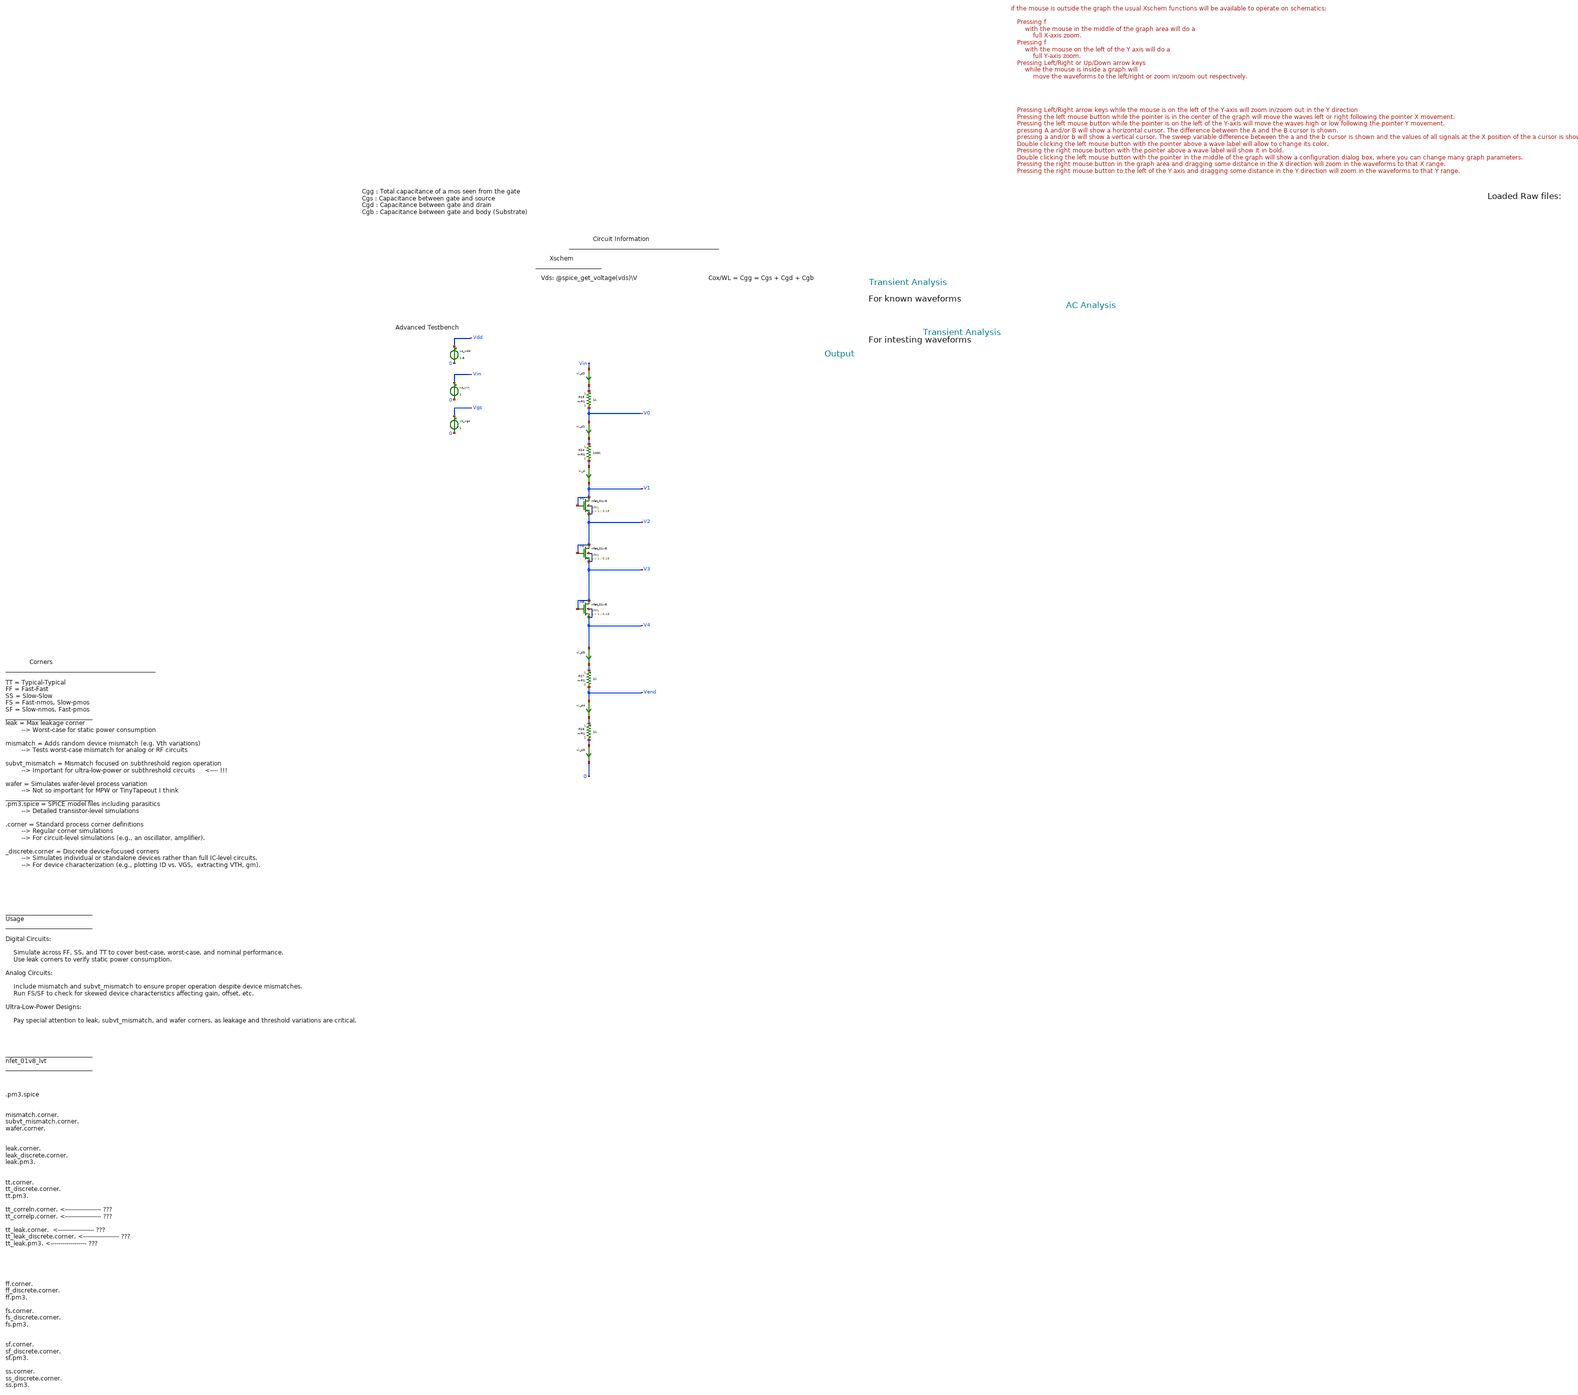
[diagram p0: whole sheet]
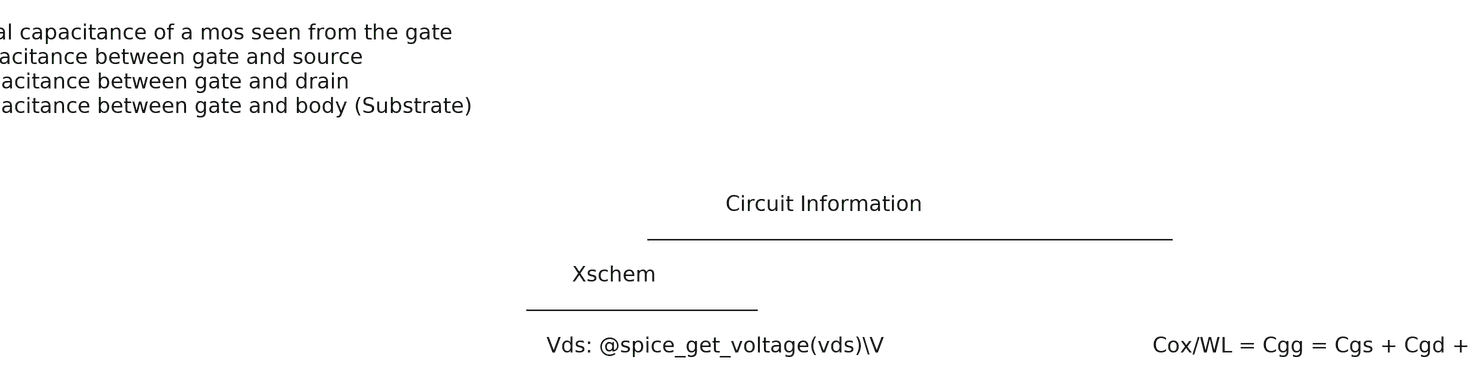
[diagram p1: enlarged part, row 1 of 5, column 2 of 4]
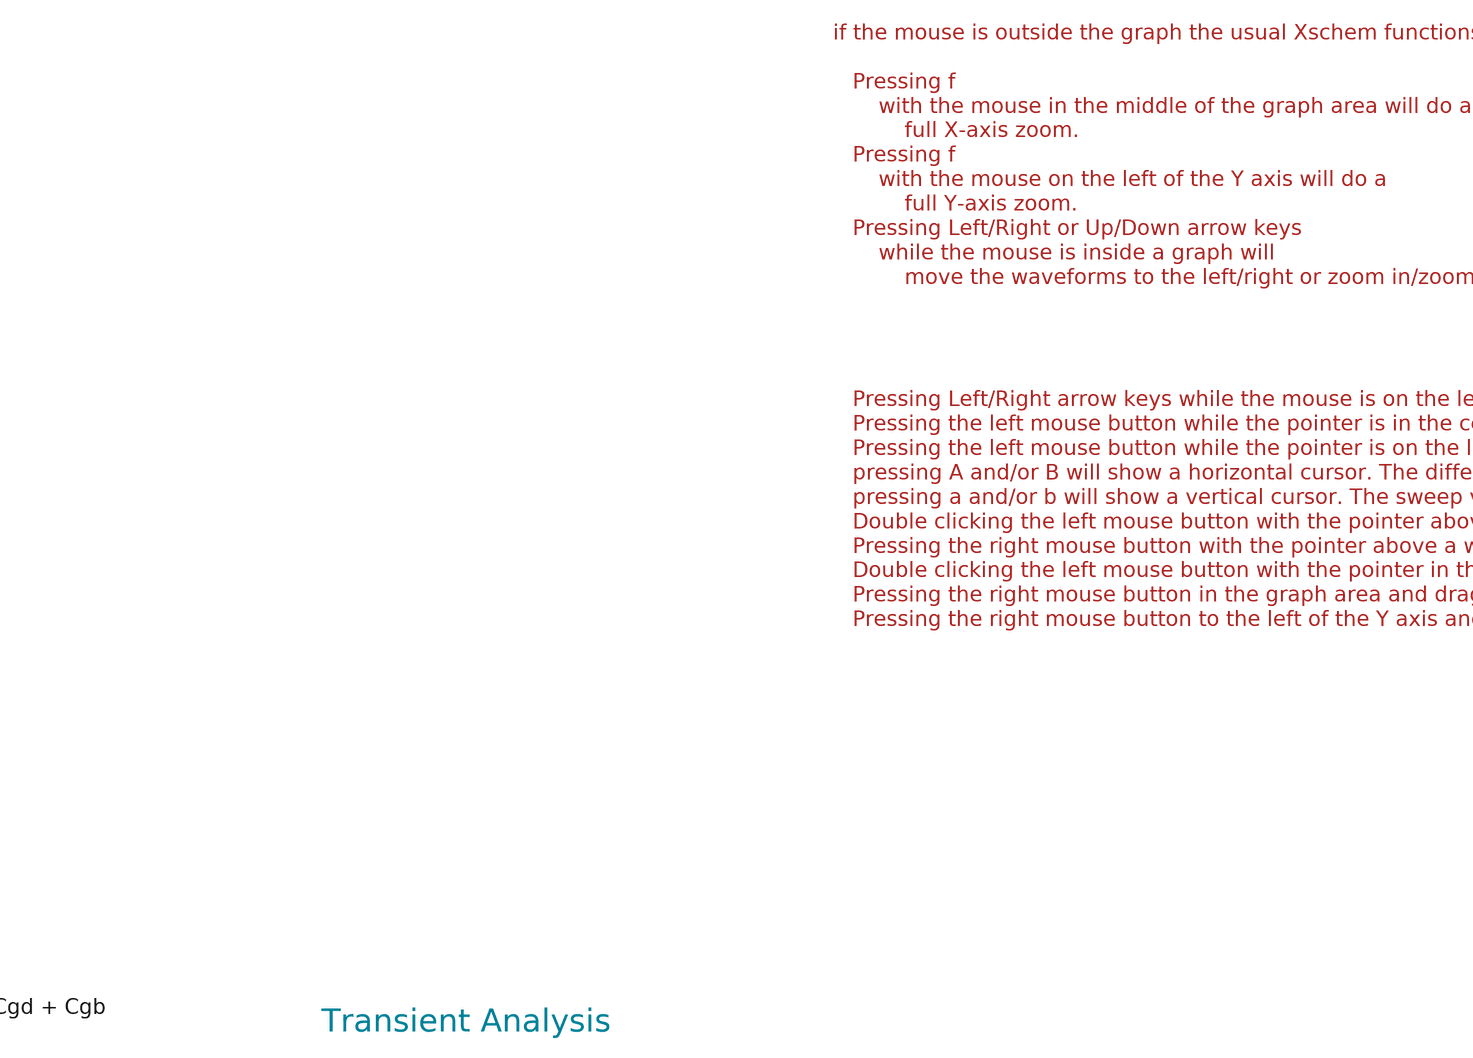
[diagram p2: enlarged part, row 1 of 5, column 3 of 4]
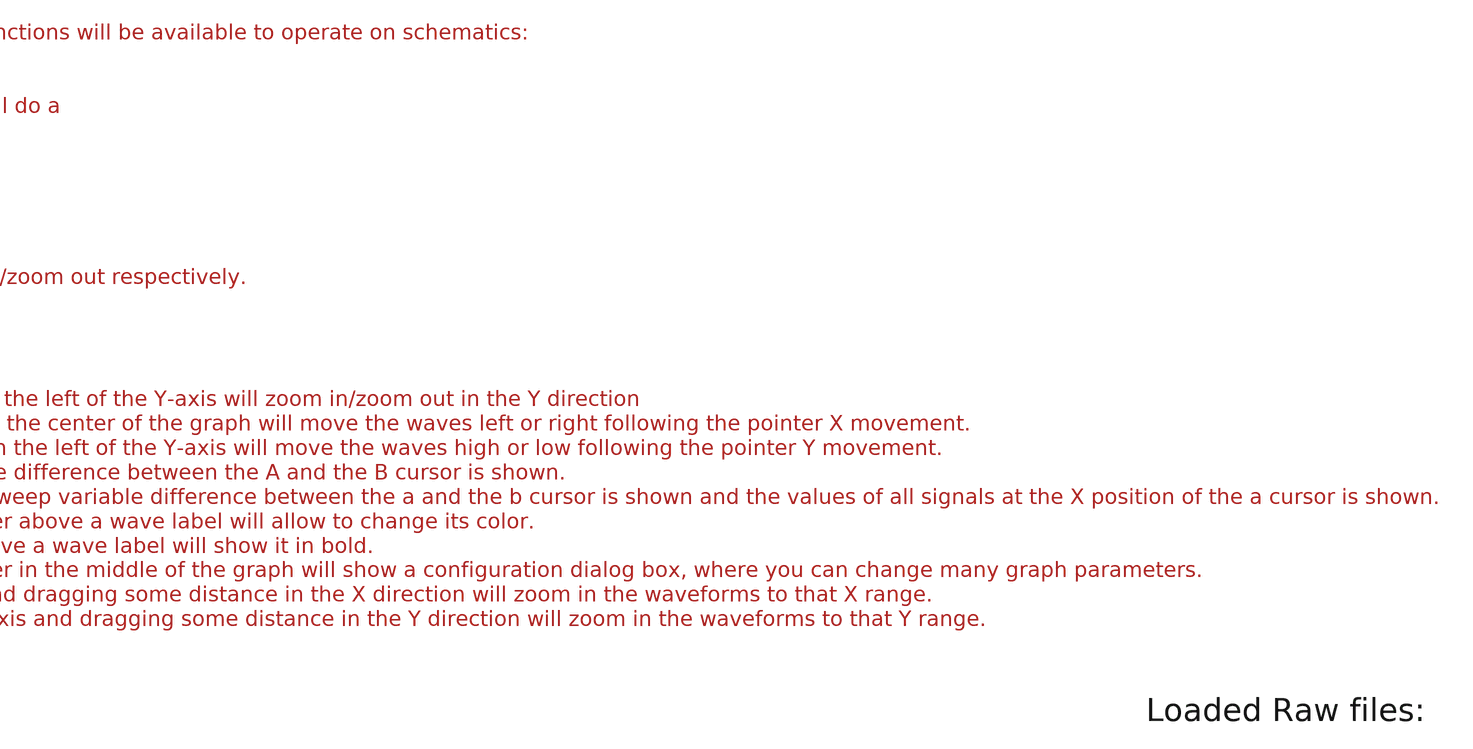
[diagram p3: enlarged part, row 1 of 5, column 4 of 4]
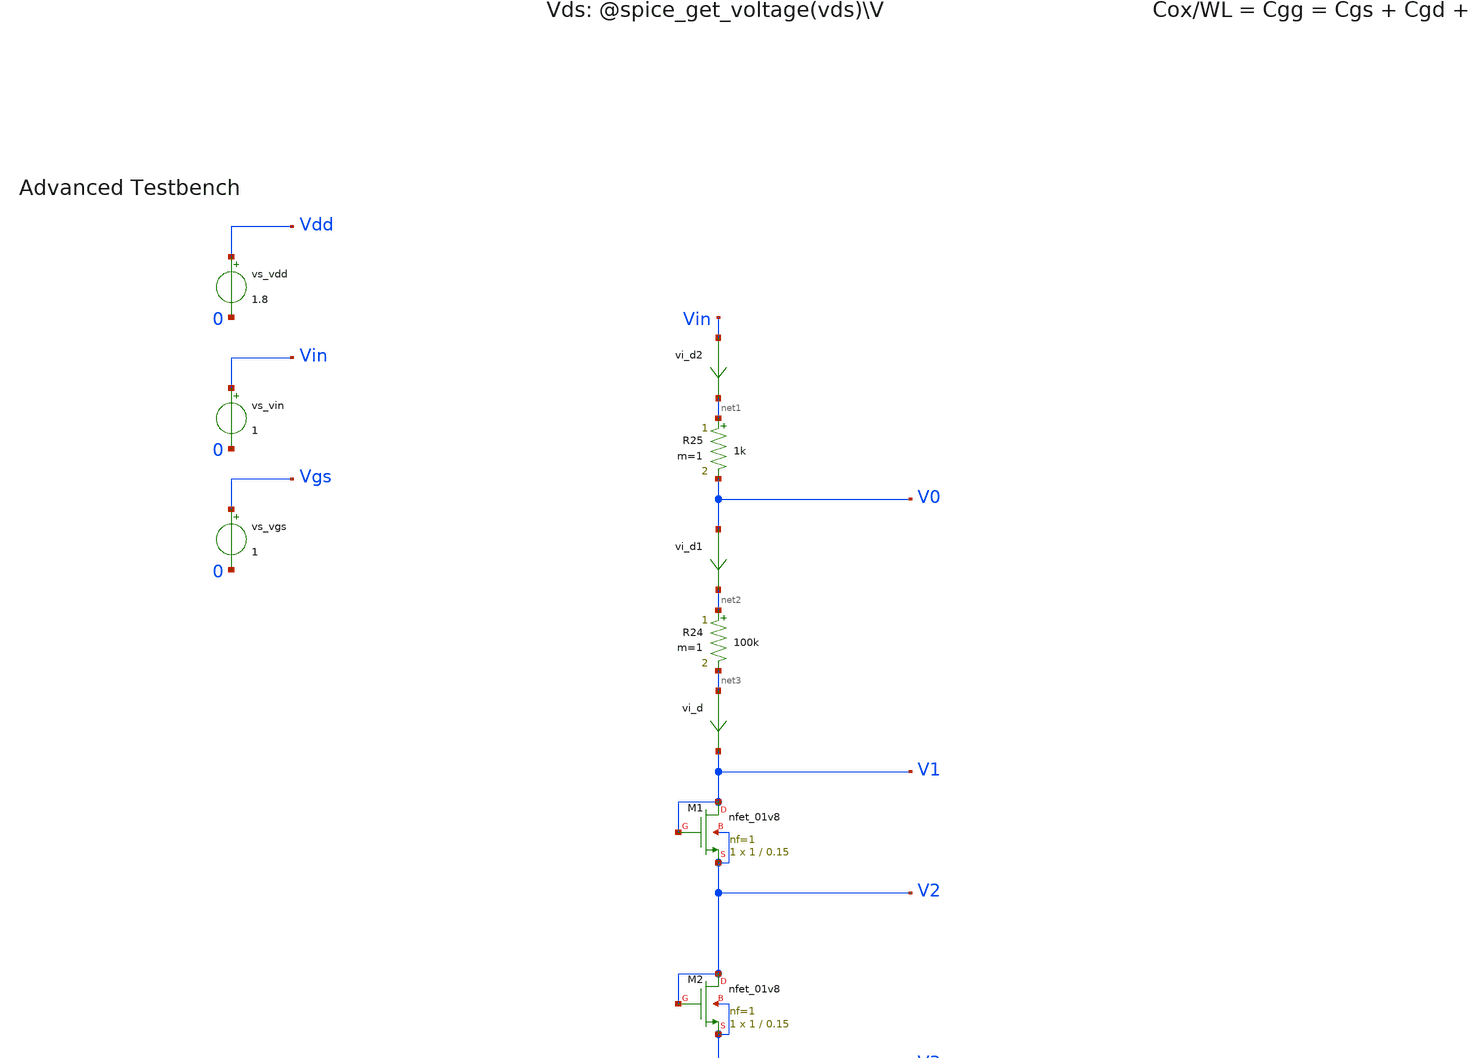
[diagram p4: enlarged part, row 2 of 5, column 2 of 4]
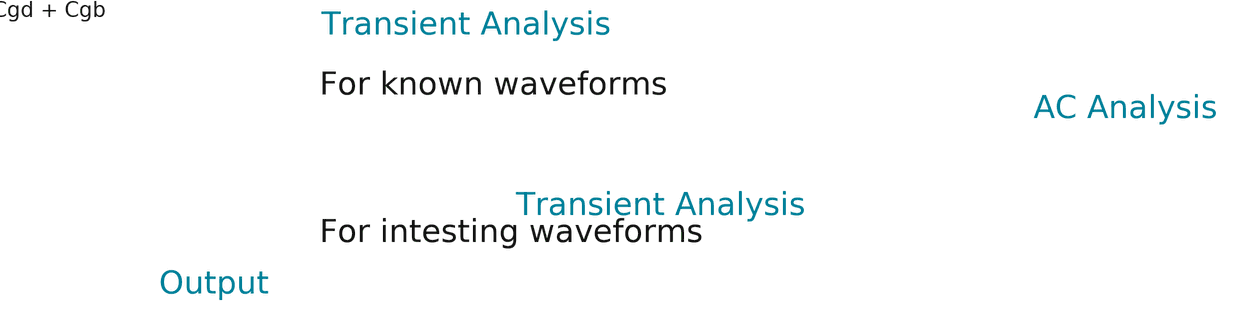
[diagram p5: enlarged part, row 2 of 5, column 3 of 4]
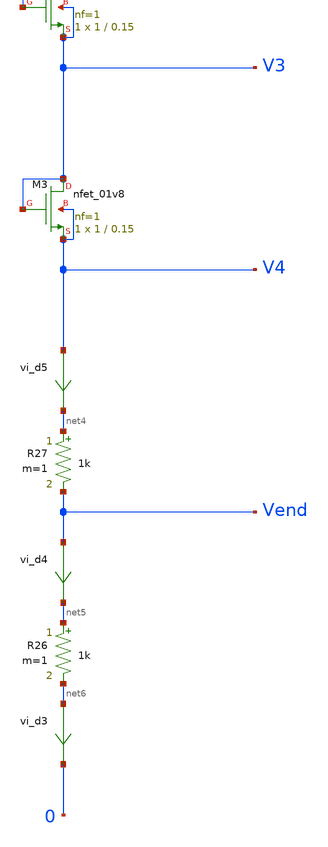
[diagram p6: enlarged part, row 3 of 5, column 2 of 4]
** sch_path: tt10-hdl/tt_um_test_commit/xschem/T0/mosDiode/nmosDiode_tb.sch
* Copyright (C) 1998-2024 Stefan Frederik Schippers
* This program is free software; you can redistribute it and/or modify
* it under the terms of the GNU General Public License as published by
* the Free Software Foundation; either version 2 of the License, or
* (at your option) any later version.
* This program is distributed in the hope that it will be useful,
* but WITHOUT ANY WARRANTY; without even the implied warranty of
* MERCHANTABILITY or FITNESS FOR A PARTICULAR PURPOSE.  See the
* GNU General Public License for more details.
* You should have received a copy of the GNU General Public License
* along with this program; if not, write to the Free Software
**.subckt nmosDiode_tb
vs_vgs Vgs 0 1
vs_vin Vin 0 1
vs_vdd Vdd 0 1.8
vi_d net3 V1 0
.save i(vi_d)
XM1 V1 V1 V2 V2 sky130_fd_pr__nfet_01v8 L=0.15 W=1 nf=1 ad='int((1 + 1)/2) * 1 / 1 * 0.29' as='int((1 + 2)/2) * 1 / 1 * 0.29'
+ pd='2*int((1 + 1)/2) * (1 / 1 + 0.29)' ps='2*int((1 + 2)/2) * (1 / 1 + 0.29)' nrd='0.29 / 1 ' nrs='0.29 / 1 '
+ sa=0 sb=0 sd=0 mult=1 m=1
R24 net2 net3 100k m=1
R25 net1 V0 1k m=1
vi_d1 V0 net2 0
.save i(vi_d1)
vi_d2 Vin net1 0
.save i(vi_d2)
vi_d3 net6 0 0
.save i(vi_d3)
R26 net5 net6 1k m=1
R27 net4 Vend 1k m=1
vi_d4 Vend net5 0
.save i(vi_d4)
vi_d5 V4 net4 0
.save i(vi_d5)
XM2 V2 V2 V3 V3 sky130_fd_pr__nfet_01v8 L=0.15 W=1 nf=1 ad='int((1 + 1)/2) * 1 / 1 * 0.29' as='int((1 + 2)/2) * 1 / 1 * 0.29'
+ pd='2*int((1 + 1)/2) * (1 / 1 + 0.29)' ps='2*int((1 + 2)/2) * (1 / 1 + 0.29)' nrd='0.29 / 1 ' nrs='0.29 / 1 '
+ sa=0 sb=0 sd=0 mult=1 m=1
XM3 V3 V3 V4 V4 sky130_fd_pr__nfet_01v8 L=0.15 W=1 nf=1 ad='int((1 + 1)/2) * 1 / 1 * 0.29' as='int((1 + 2)/2) * 1 / 1 * 0.29'
+ pd='2*int((1 + 1)/2) * (1 / 1 + 0.29)' ps='2*int((1 + 2)/2) * (1 / 1 + 0.29)' nrd='0.29 / 1 ' nrs='0.29 / 1 '
+ sa=0 sb=0 sd=0 mult=1 m=1
**** begin user architecture code



.temp 30

.param nw = 2
.param nl = 0.3
.param pw = 1
.param pl = 0.6

*.option gmin=5n
*.option scale=1e-6
*.option wnflag=1
.option savecurrents

.save all
.control
  save all alli

  save @m.xm1.msky130_fd_pr__nfet_01v8[gm]
  save @m.xm1.msky130_fd_pr__nfet_01v8[id]
  save @m.xm1.msky130_fd_pr__nfet_01v8[vgs]

  save @m.xm1.msky130_fd_pr__nfet_01v8[cgg]
  save @m.xm1.msky130_fd_pr__nfet_01v8[cgs]
  save @m.xm1.msky130_fd_pr__nfet_01v8[cgd]
  save @m.xm1.msky130_fd_pr__nfet_01v8[cgb]

  save @m.xm1.msky130_fd_pr__nfet_01v8[vds]
  save @m.xm1.msky130_fd_pr__nfet_01v8[vdsat]
  save @m.xm1.msky130_fd_pr__nfet_01v8[vth]


  save @m.xm1.msky130_fd_pr__nfet_01v8[leff]
  save @m.xm1.msky130_fd_pr__nfet_01v8[weff]
  save @m.xm1.msky130_fd_pr__nfet_01v8[gds]
  save @m.xm1.msky130_fd_pr__nfet_01v8[l]
  save @m.xm1.msky130_fd_pr__nfet_01v8[w]
  save @m.xm1.msky130_fd_pr__nfet_01v8[gm]
  save @m.xm1.msky130_fd_pr__nfet_01v8[gm]
  save @m.xm1.msky130_fd_pr__nfet_01v8[gm]
  save @m.xm1.msky130_fd_pr__nfet_01v8[gm]
  save @m.xm1.msky130_fd_pr__nfet_01v8[gm]


  dc vs_vin 0 1.8  0.005
  *dc v_dev_vds 0 20u  10n
  write nmos_tb.raw


  op
  set appendwrite
  write nmos_tb.raw



  *tran 1n 5u
  *write nmos_tb.raw






  *quit 0




.endc





** opencircuitdesign pdks install
.lib $::SKYWATER_MODELS/sky130.lib.spice tt
.include $::SKYWATER_STDCELLS/sky130_fd_sc_hd.spice


**** end user architecture code
**.ends
.end
